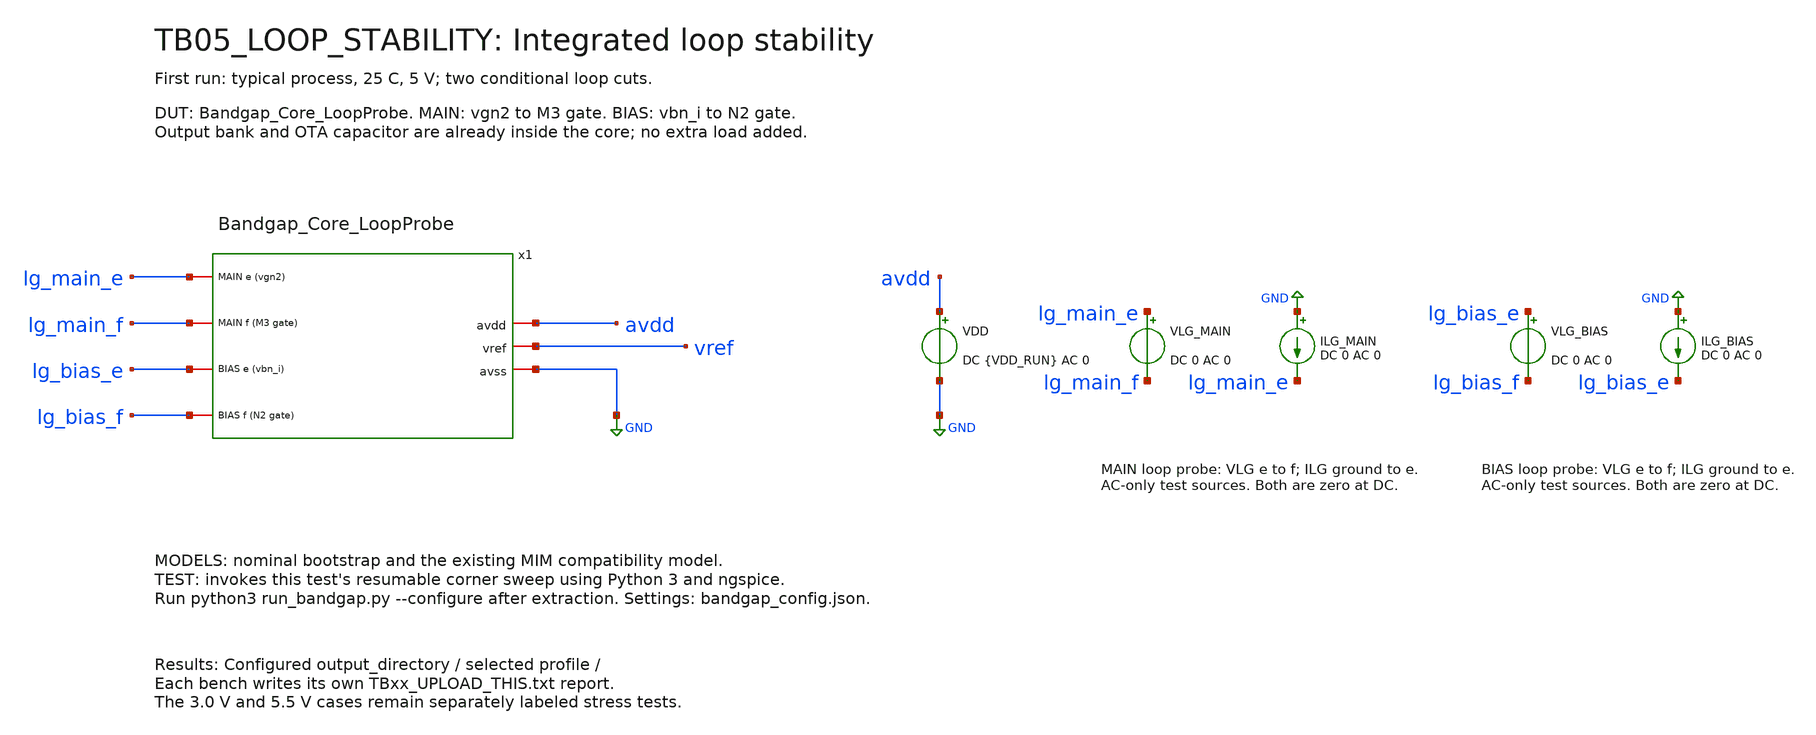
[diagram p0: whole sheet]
** sch_path: TB05_LOOP_STABILITY.sch
**.subckt TB05_LOOP_STABILITY
VDD avdd GND DC {VDD_RUN} AC 0
VLG_MAIN lg_main_e lg_main_f DC 0 AC 0
ILG_MAIN GND lg_main_e DC 0 AC 0
VLG_BIAS lg_bias_e lg_bias_f DC 0 AC 0
ILG_BIAS GND lg_bias_e DC 0 AC 0
x1 avdd vref GND lg_main_e lg_main_f lg_bias_e lg_bias_f Bandgap_Core_LoopProbe
**** begin user architecture code

* TB_PVT_MODELS_BEGIN
.include /foss/pdks/gf180mcuD/libs.tech/ngspice/design.ngspice
.lib /foss/pdks/gf180mcuD/libs.tech/ngspice/sm141064.ngspice typical
.lib /foss/pdks/gf180mcuD/libs.tech/ngspice/sm141064.ngspice bjt_typical
.lib /foss/pdks/gf180mcuD/libs.tech/ngspice/sm141064.ngspice res_typical
* GF180 2p0fF MIM fit, charge-form ngspice compatibility implementation.
* Derived from GlobalFoundries PDK Authors (2022), Apache-2.0:
* https://github.com/google/globalfoundries-pdk-libs-gf180mcu_fd_pr
* Same geometry, voltage/temperature coefficients, leakage and corner factors.
* Differential C(V)=C0*(1+a*V+b*V^2) is implemented as
* Q(V)=C0*(V+a*V^2/2+b*V^3/3), so dQ/dV exactly equals C(V).
* This avoids ngspice's poorly scaled unity-capacitor C-expression expansion.
* Do not also include mimcap_typical: it would redefine cap_mim_2f0fF.
.param mim_corner_2p0fF=1 mc_c_cox_2p0fF=0
.subckt cap_mim_2f0fF  1 2  c_length=l  c_width=w dtemp=0 par=1
.param gleak='9.51e-10/5*10000'
.param c_cox='1.99e-3*mim_corner_2p0fF'
.param c_capsw='2.383e-10*mim_corner_2p0fF'
.param c_vcr1='0+(c_width>5u||c_length>5u)*8.742e-6+(c_width<=5u||c_length<=5u)*(-81e-6)'
.param c_vcr2='0+(c_width>5u||c_length>5u)*9.188e-6+(c_width<=5u||c_length<=5u)*(16.7e-6)'

.param c_tnom=25
.param c_tc1=1.46e-5
.param c_tc2=-5.55e-8
.param c_AREA='c_length*c_width'
.param c_PERI='2*(c_length+c_width)'

.param c_c0='(c_cox*c_AREA+c_capsw*c_PERI)*(1+c_tc1*(temper +dtemp -c_tnom)+c_tc2*(temper+dtemp-c_tnom)*(temper+dtemp-c_tnom))'
*
c_cap 1 2 Q='c_c0*(v(1,2)+c_vcr1*v(1,2)*v(1,2)/2+c_vcr2*v(1,2)*v(1,2)*v(1,2)/3)*(1+mc_c_cox_2p0fF)'
r_leak 1 2 r='1/(gleak*c_AREA)' tc1=c_tc1 tc2=c_tc2 dtemp=dtemp
.ends cap_mim_2f0fF
* Bootstrap nominal process; runner selects each corner independently. Mismatch disabled. MIM compatibility model above is intentional.
.options tnom=25 numdgt=15 method=trap
.param sw_stat_global=0 sw_stat_mismatch=0 fnoicor=0
.param VDD_RUN=5
.temp 25
* TB_PVT_MODELS_END


.control
set noaskquit
echo BANDGAP_SINGLE_RUNNER_V9_TB05_LOOP_STABILITY
shell python3 /foss/designs/chipalooza-bandgap/Jonah_Saunders_Bandgap/run_bandgap.py --deck /headless/.xschem/simulations/TB05_LOOP_STABILITY.spice --test TB05_LOOP_STABILITY
echo RUNNER_RETURNED_CHECK_REPORT_AND_ERRORS
.endc

**** end user architecture code
**.ends
.GLOBAL GND
.end
